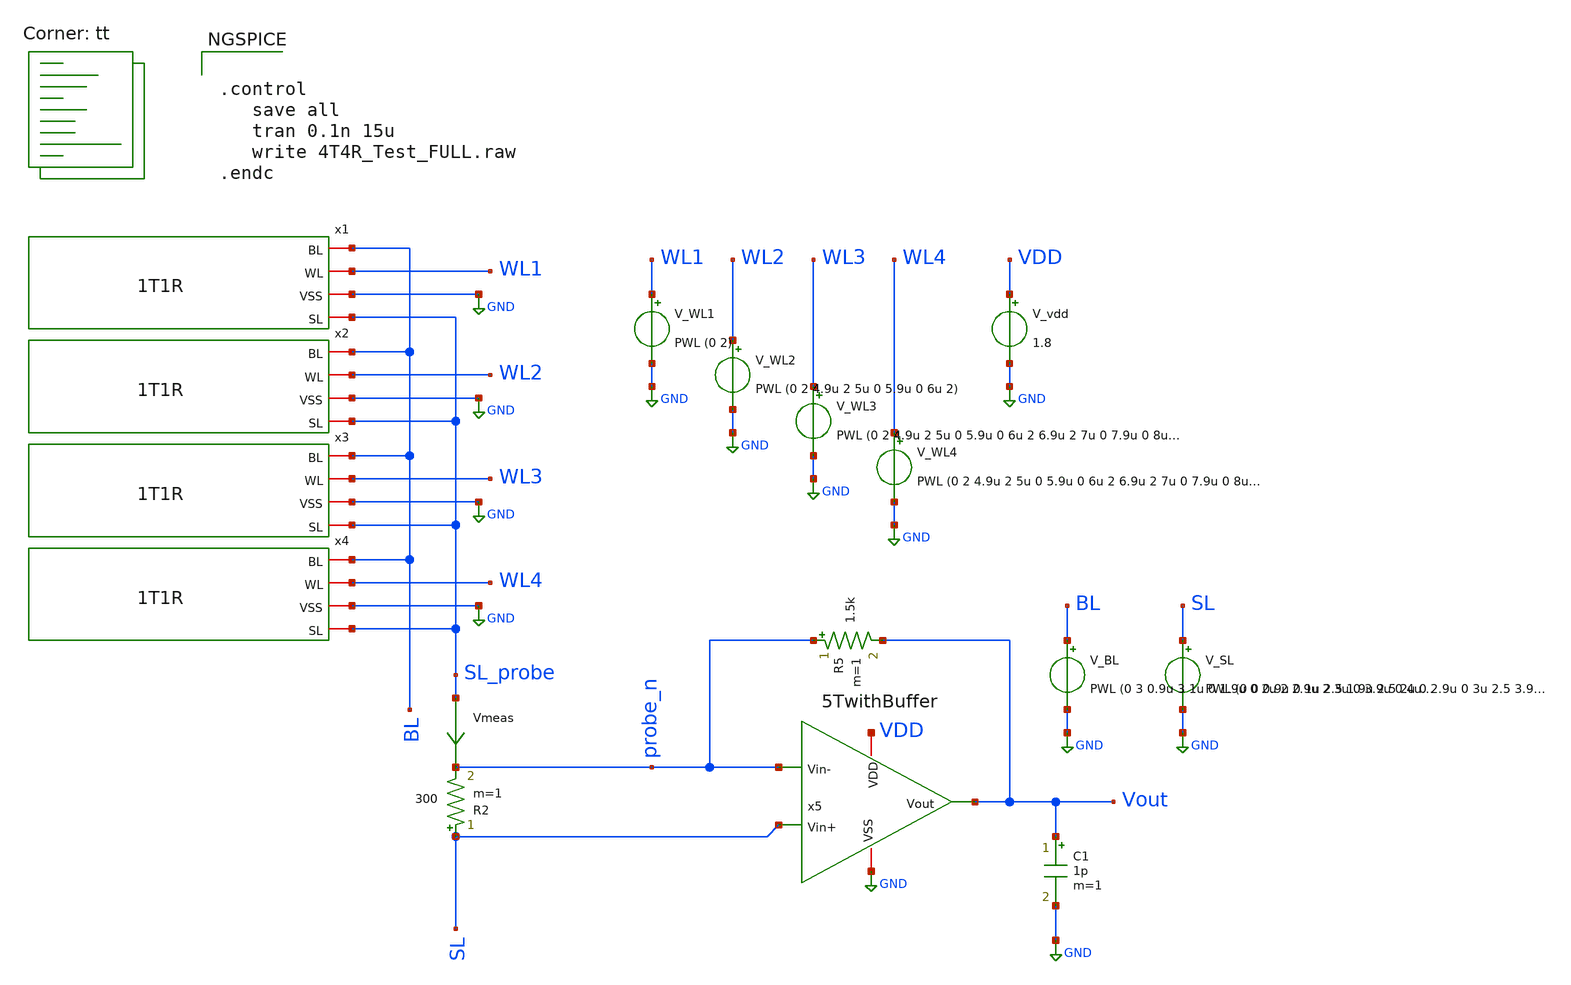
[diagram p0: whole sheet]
** sch_path: xschem/test/xschem/4T4R_Test_FULL.sch
* StefanSchippers/xschem_sky130/sky130_fd_pr/reram.sym:
* Copyright 2021 Stefan Frederik Schippers
* Licensed under the Apache License, Version 2.0 (the "License");
**.subckt 4T4R_Test_FULL
x1 BL WL1 SL_probe GND 1T1R
x2 BL WL2 SL_probe GND 1T1R
x3 BL WL3 SL_probe GND 1T1R
x4 BL WL4 SL_probe GND 1T1R
V_WL1 WL1 GND PWL (0 2)
V_WL2 WL2 GND PWL (0 2 4.9u 2 5u 0 5.9u 0 6u 2)
V_WL3 WL3 GND PWL (0 2 4.9u 2 5u 0 5.9u 0 6u 2 6.9u 2 7u 0 7.9u 0 8u 2)
V_WL4 WL4 GND PWL (0 2 4.9u 2 5u 0 5.9u 0 6u 2 6.9u 2 7u 0 7.9u 0 8u 2 8.9u 2 9u 0 9.9u 0 10u 2)
V_SL SL GND PWL (0 0 0.9u 0 1u 2.5 1.9u 2.5 2u 0 2.9u 0 3u 2.5 3.9u 2.5 4u 0)
V_BL BL GND PWL (0 3 0.9u 3 1u 0 1.9u 0 2u 2 2.9u 2 3u 0 3.9u 0 4u 0.2 4.9u 0.2 5u 2 5.9u 2 6u 0.2
+ 6.9u 0.2 7u 2 7.9u 2 8u 0.2 8.9u 0.2 9u 2 9.9u 2 10u 0.2 10.9u 0.2 11u 2 11.9u 2 12u 0.2)
x5 VDD Vout probe_n SL GND 5TwithBuffer
R2 SL probe_n 300 m=1
C1 Vout GND 1p m=1
R5 probe_n Vout 1.5k m=1
V_vdd VDD GND 1.8
Vmeas SL_probe probe_n 0
.save i(vmeas)
**** begin user architecture code
.lib $::SKYWATER_MODELS/sky130.lib.spice tt


.control
   save all
   tran 0.1n 15u
   write 4T4R_Test_FULL.raw
.endc


**** end user architecture code
**.ends

* expanding   symbol:  1T1R.sym # of pins=4
** sym_path: xschem/test/xschem/1T1R.sym
** sch_path: xschem/test/xschem/1T1R.sch
.subckt 1T1R BL WL SL VSS
*.iopin SL
*.iopin WL
*.iopin BL
*.iopin VSS
XR1 BL net1 sky130_fd_pr_reram__reram_cell Tfilament_0=3.8e-9
XM1 net1 WL SL VSS sky130_fd_pr__nfet_g5v0d10v5 L=0.5 W=7 nf=1 ad='int((nf+1)/2) * W/nf * 0.29' as='int((nf+2)/2) * W/nf * 0.29'
+ pd='2*int((nf+1)/2) * (W/nf + 0.29)' ps='2*int((nf+2)/2) * (W/nf + 0.29)' nrd='0.29 / W' nrs='0.29 / W'
+ sa=0 sb=0 sd=0 mult=1 m=1
.ends


* expanding   symbol:  amplifiers/dec24/5TwithBuffer.sym # of pins=5
** sym_path: amplifiers/dec24/5TwithBuffer.sym
** sch_path: amplifiers/dec24/5TwithBuffer.sch
.subckt 5TwithBuffer VDD Vout Vin- Vin+ VSS
*.iopin VDD
*.iopin VSS
*.ipin Vin-
*.ipin Vin+
*.opin Vout
I0 VDD Vb1 100u
XM1 net1 Vin+ Vsink VSS sky130_fd_pr__nfet_01v8 L=1 W=4 nf=1 ad='int((nf+1)/2) * W/nf * 0.29' as='int((nf+2)/2) * W/nf * 0.29'
+ pd='2*int((nf+1)/2) * (W/nf + 0.29)' ps='2*int((nf+2)/2) * (W/nf + 0.29)' nrd='0.29 / W' nrs='0.29 / W'
+ sa=0 sb=0 sd=0 mult=1 m=1
XM2 Vout Vin- Vsink VSS sky130_fd_pr__nfet_01v8 L=1 W=4 nf=1 ad='int((nf+1)/2) * W/nf * 0.29' as='int((nf+2)/2) * W/nf * 0.29'
+ pd='2*int((nf+1)/2) * (W/nf + 0.29)' ps='2*int((nf+2)/2) * (W/nf + 0.29)' nrd='0.29 / W' nrs='0.29 / W'
+ sa=0 sb=0 sd=0 mult=1 m=1
XM3 Vb1 Vb1 VSS VSS sky130_fd_pr__nfet_01v8 L=1 W=5 nf=1 ad='int((nf+1)/2) * W/nf * 0.29' as='int((nf+2)/2) * W/nf * 0.29'
+ pd='2*int((nf+1)/2) * (W/nf + 0.29)' ps='2*int((nf+2)/2) * (W/nf + 0.29)' nrd='0.29 / W' nrs='0.29 / W'
+ sa=0 sb=0 sd=0 mult=1 m=1
XM4 Vsink Vb1 VSS VSS sky130_fd_pr__nfet_01v8 L=1 W=5 nf=1 ad='int((nf+1)/2) * W/nf * 0.29' as='int((nf+2)/2) * W/nf * 0.29'
+ pd='2*int((nf+1)/2) * (W/nf + 0.29)' ps='2*int((nf+2)/2) * (W/nf + 0.29)' nrd='0.29 / W' nrs='0.29 / W'
+ sa=0 sb=0 sd=0 mult=1 m=1
XM7 VDD Vout net2 VSS sky130_fd_pr__nfet_01v8 L=1 W=20 nf=1 ad='int((nf+1)/2) * W/nf * 0.29' as='int((nf+2)/2) * W/nf * 0.29'
+ pd='2*int((nf+1)/2) * (W/nf + 0.29)' ps='2*int((nf+2)/2) * (W/nf + 0.29)' nrd='0.29 / W' nrs='0.29 / W'
+ sa=0 sb=0 sd=0 mult=1 m=1
XM8 net2 Vb1 VSS VSS sky130_fd_pr__nfet_01v8 L=1 W=5 nf=1 ad='int((nf+1)/2) * W/nf * 0.29' as='int((nf+2)/2) * W/nf * 0.29'
+ pd='2*int((nf+1)/2) * (W/nf + 0.29)' ps='2*int((nf+2)/2) * (W/nf + 0.29)' nrd='0.29 / W' nrs='0.29 / W'
+ sa=0 sb=0 sd=0 mult=5 m=5
XM5 net1 net1 VDD VDD sky130_fd_pr__pfet_01v8_lvt L=1 W=10 nf=1 ad='int((nf+1)/2) * W/nf * 0.29' as='int((nf+2)/2) * W/nf * 0.29'
+ pd='2*int((nf+1)/2) * (W/nf + 0.29)' ps='2*int((nf+2)/2) * (W/nf + 0.29)' nrd='0.29 / W' nrs='0.29 / W'
+ sa=0 sb=0 sd=0 mult=1 m=1
XM6 VDD net1 Vout VDD sky130_fd_pr__pfet_01v8_lvt L=1 W=10 nf=1 ad='int((nf+1)/2) * W/nf * 0.29' as='int((nf+2)/2) * W/nf * 0.29'
+ pd='2*int((nf+1)/2) * (W/nf + 0.29)' ps='2*int((nf+2)/2) * (W/nf + 0.29)' nrd='0.29 / W' nrs='0.29 / W'
+ sa=0 sb=0 sd=0 mult=1 m=1
.ends

.GLOBAL GND
.GLOBAL VDD
**** begin user architecture code

.subckt sky130_fd_pr_reram__reram_cell TE BE Tfilament_0=3.3e-9 area_ox=0.1024e-12
N1 TE BE nFilament sky130_fd_pr_reram__reram_model
.ic v(nFilament)={Tfilament_0*1.0e9}
.ends sky130_fd_pr_reram__reram_cell

.model sky130_fd_pr_reram__reram_model sky130_fd_pr_reram__reram_module  area_ox = 0.1024e-12  Tox =
+ 5.0  Tfilament_max = 4.9  Tfilament_min = 3.3  Eact_generation = 1.501  Eact_recombination  = 1.500
+  I_k1  = 6.140e-5  Tfilament_ref = 4.7249  V_ref = 0.430  velocity_k1 = 150  gamma_k0  = 16.5  gamma_k1
+  = -1.25  Temperature_0 = 300  C_thermal = 3.1825e-16  tau_thermal = 0.23e-9  t_step  = 1.0e-9
+  smoothing = 1e-7  Kclip = 200

.control
pre_osdi $SKYWATER_MODELS/sky130_fd_pr_reram__reram_module.osdi
.endc

**** end user architecture code
.end
